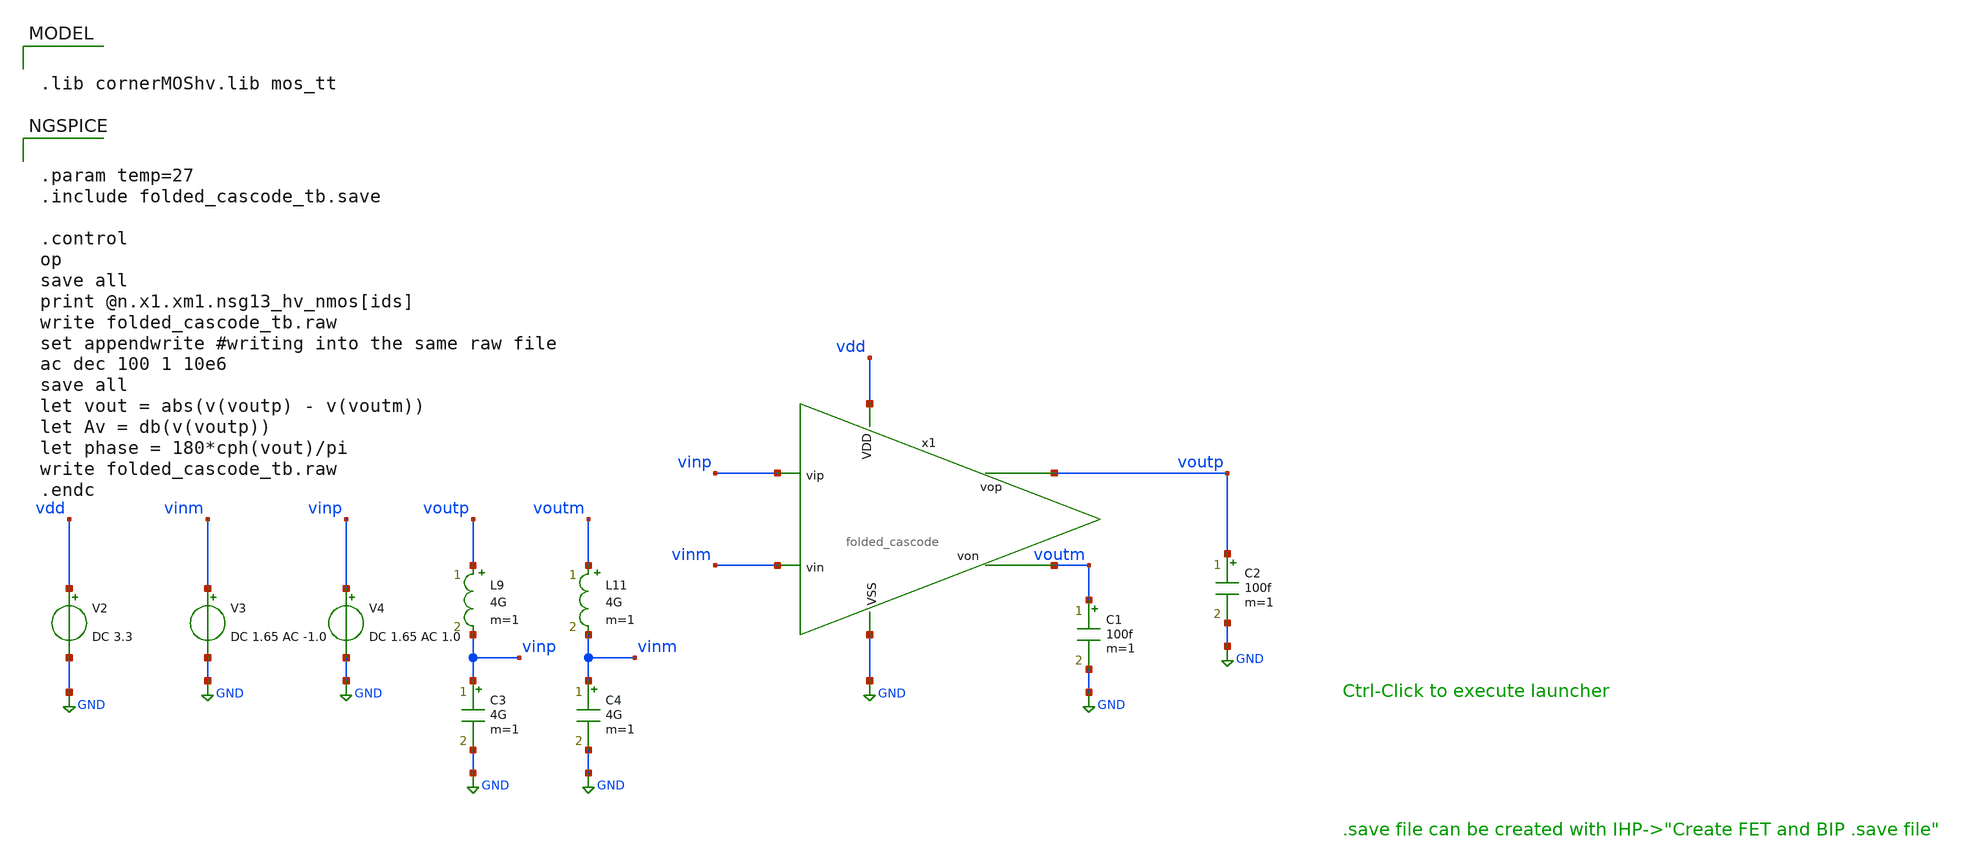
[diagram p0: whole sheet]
** sch_path: testbench/folded_cascode/folded_cascode_tb.sch
**.subckt folded_cascode_tb
C1 voutm GND 100f m=1
C2 voutp GND 100f m=1
V2 vdd GND DC 3.3
V3 vinm GND DC 1.65 AC -1.0
V4 vinp GND DC 1.65 AC 1.0
L9 voutp vinp 4G m=1
C3 vinp GND 4G m=1
L11 voutm vinm 4G m=1
C4 vinm GND 4G m=1
x1 vdd voutp voutm vinp vinm GND folded_cascode
**** begin user architecture code

.lib cornerMOShv.lib mos_tt



.param temp=27
.include folded_cascode_tb.save

.control
op
save all
print @n.x1.xm1.nsg13_hv_nmos[ids]
write folded_cascode_tb.raw
set appendwrite #writing into the same raw file
ac dec 100 1 10e6
save all
let vout = abs(v(voutp) - v(voutm))
let Av = db(v(voutp))
let phase = 180*cph(vout)/pi
write folded_cascode_tb.raw
.endc


**** end user architecture code
**.ends

* expanding   symbol:  folded_cascode.sym # of pins=6
** sym_path: schematic/folded_cascode.sym
** sch_path: schematic/folded_cascode.sch
.subckt folded_cascode VDD vop von vip vin VSS
*.ipin VDD
*.ipin vip
*.ipin vin
*.opin vop
*.opin von
*.ipin VSS
XM1 net2 vip net1 net1 sg13_hv_nmos w=0.3u l=0.45u ng=1 m=1 mm_ok=1
XM2 net2 pbias_upper VDD VDD sg13_hv_pmos w=0.3u l=0.4u ng=1 m=1 mm_ok=1
XM3 net3 vin net1 net1 sg13_hv_nmos w=0.3u l=0.45u ng=1 m=1 mm_ok=1
XM4 net1 tail_bias VSS VSS sg13_hv_nmos w=0.3u l=0.45u ng=1 m=1 mm_ok=1
XM6 net3 pbias_upper VDD VDD sg13_hv_pmos w=0.3u l=0.4u ng=1 m=1 mm_ok=1
XM7 von pbias_lower net2 net2 sg13_hv_pmos w=0.3u l=0.4u ng=1 m=1 mm_ok=1
XM8 vop pbias_lower net3 net3 sg13_hv_pmos w=0.3u l=0.4u ng=1 m=1 mm_ok=1
XM9 vop nbias_upper net5 net5 sg13_hv_nmos w=0.3u l=0.45u ng=1 m=1 mm_ok=1
XM5 von nbias_upper net4 net4 sg13_hv_nmos w=0.3u l=0.45u ng=1 m=1 mm_ok=1
XM10 net5 nbias_lower VSS VSS sg13_hv_nmos w=0.3u l=0.45u ng=1 m=1 mm_ok=1
XM11 net4 nbias_lower VSS VSS sg13_hv_nmos w=0.3u l=0.45u ng=1 m=1 mm_ok=1
V1 tail_bias VSS 3
V2 pbias_upper VSS 3
V3 pbias_lower VSS 3
V4 nbias_upper VSS 3
V5 nbias_lower VSS 3
.ends

.GLOBAL GND
.end
